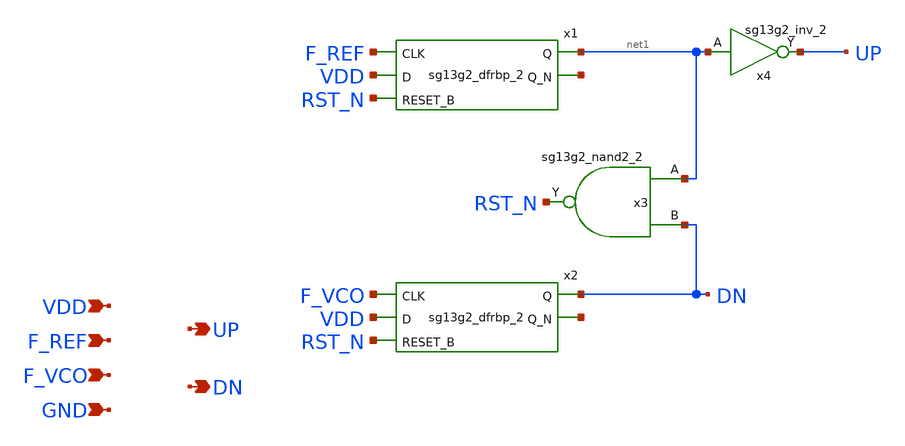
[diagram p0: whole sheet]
** sch_path: schematic/phase-freq-detector/PFD.sch
* IHP-GmbH/IHP-Open-PDK/ihp-sg13g2/libs.tech/xschem/sg13g2_stdcells/sg13g2_inv_2.sch:
* Copyright 2023 IHP PDK Authors
* Licensed under the Apache License, Version 2.0 (the "License");
**.subckt PFD UP F_REF VDD GND DN F_VCO
*.opin UP
*.ipin F_REF
*.ipin VDD
*.ipin GND
*.opin DN
*.ipin F_VCO
x1 net1 net2 F_REF VDD RST_N VDD GND sg13g2_dfrbp_2
x2 DN net3 F_VCO VDD RST_N VDD GND sg13g2_dfrbp_2
x3 RST_N net1 DN VDD GND sg13g2_nand2_2
x4 UP net1 VDD GND sg13g2_inv_2
**.ends

* expanding   symbol:  sg13g2_stdcells/sg13g2_inv_2.sym # of pins=2
** sym_path: sg13g2_stdcells/sg13g2_inv_2.sym
** sch_path: sg13g2_stdcells/sg13g2_inv_2.sch
.subckt sg13g2_inv_2 Y A VDD VSS
*.opin Y
*.ipin A
*.iopin VDD
*.iopin VSS
XM1 Y A VSS VSS sg13_lv_nmos w=1.48u l=130.00n ng=2 m=1 mm_ok=1
XM2 Y A VDD VDD sg13_lv_pmos w=2.24u l=130.00n ng=2 m=1 mm_ok=1
.ends

.end
